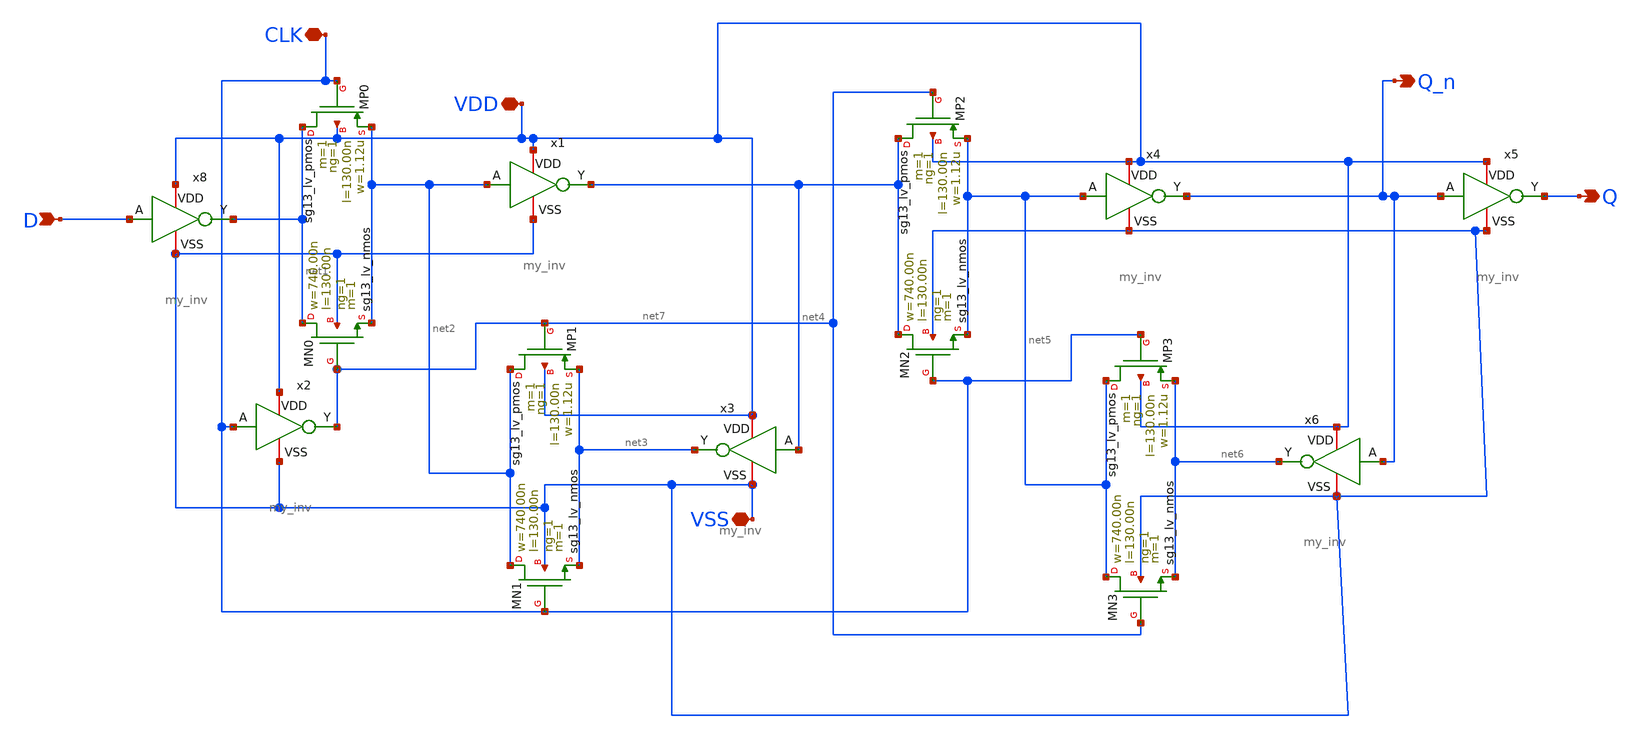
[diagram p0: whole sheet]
** sch_path: XSCHEM/flipflopn.sch
**.subckt flipflopn D Q CLK VDD VSS Q_n
*.ipin D
*.opin Q
*.iopin CLK
*.iopin VDD
*.iopin VSS
*.opin Q_n
XMN0 net1 net7 net2 VSS sg13_lv_nmos w=740.00n l=130.00n ng=1 m=1 mm_ok=1
XMP0 net1 CLK net2 VDD sg13_lv_pmos w=1.12u l=130.00n ng=1 m=1 mm_ok=1
XMN1 net2 CLK net3 VSS sg13_lv_nmos w=740.00n l=130.00n ng=1 m=1 mm_ok=1
XMP1 net2 net7 net3 VDD sg13_lv_pmos w=1.12u l=130.00n ng=1 m=1 mm_ok=1
XMN2 net4 CLK net5 VSS sg13_lv_nmos w=740.00n l=130.00n ng=1 m=1 mm_ok=1
XMP2 net4 net7 net5 VDD sg13_lv_pmos w=1.12u l=130.00n ng=1 m=1 mm_ok=1
XMN3 net5 net7 net6 VSS sg13_lv_nmos w=740.00n l=130.00n ng=1 m=1 mm_ok=1
XMP3 net5 CLK net6 VDD sg13_lv_pmos w=1.12u l=130.00n ng=1 m=1 mm_ok=1
x8 VDD net1 D VSS my_inv
x1 VDD net4 net2 VSS my_inv
x2 VDD net7 CLK VSS my_inv
x3 VDD net3 net4 VSS my_inv
x4 VDD Q_n net5 VSS my_inv
x5 VDD Q Q_n VSS my_inv
x6 VDD net6 Q_n VSS my_inv
**.ends

* expanding   symbol:  my_inv.sym # of pins=4
** sym_path: xschem/my_inv.sym
** sch_path: xschem/my_inv.sch
.subckt my_inv VDD Y A VSS
*.opin Y
*.ipin A
*.iopin VDD
*.iopin VSS
XMN0 Y A VSS VSS sg13_lv_nmos w=740.00n l=130.00n ng=1 m=1 mm_ok=1
XMP0 Y A VDD VDD sg13_lv_pmos w=1.12u l=130.00n ng=1 m=1 mm_ok=1
.ends

.end
